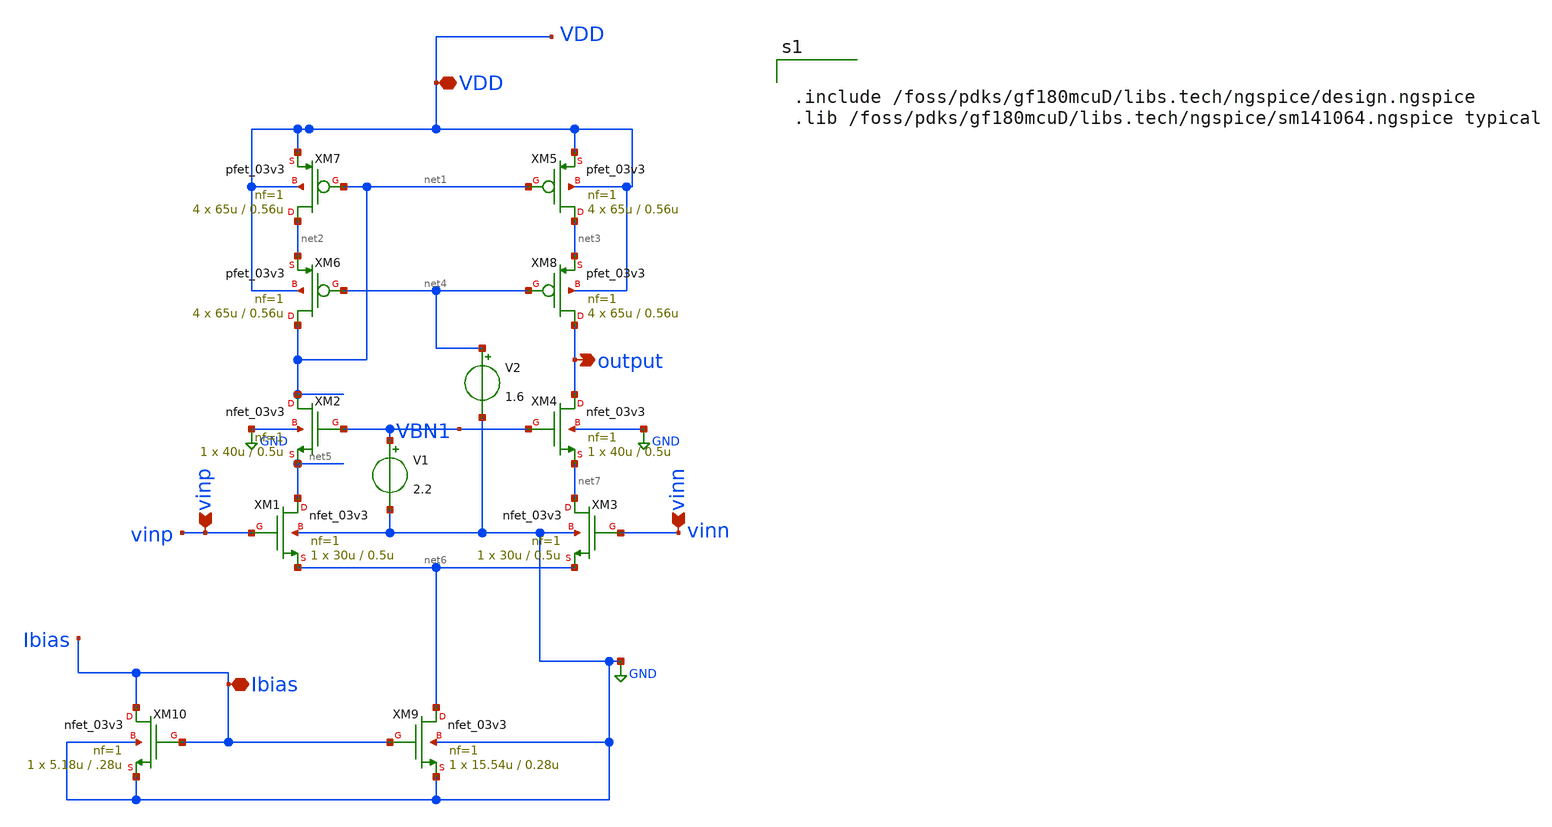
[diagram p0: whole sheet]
** sch_path: designs/libs/core_amps/ota_telescopic/telescopic_cascode.sch
**.subckt telescopic_cascode vinp vinn output Ibias VDD
*.ipin vinp
*.ipin vinn
*.opin output
*.iopin Ibias
*.iopin VDD
XM8 output net4 net3 VDD pfet_03v3 L=0.56u W=65u nf=1 ad='int((nf+1)/2) * W/nf * 0.18u' as='int((nf+2)/2) * W/nf * 0.18u'
+ pd='2*int((nf+1)/2) * (W/nf + 0.18u)' ps='2*int((nf+2)/2) * (W/nf + 0.18u)' nrd='0.18u / W' nrs='0.18u / W'
+ sa=0 sb=0 sd=0 m=4
XM4 output VBN1 net7 GND nfet_03v3 L=0.5u W=40u nf=1 ad='int((nf+1)/2) * W/nf * 0.18u' as='int((nf+2)/2) * W/nf * 0.18u'
+ pd='2*int((nf+1)/2) * (W/nf + 0.18u)' ps='2*int((nf+2)/2) * (W/nf + 0.18u)' nrd='0.18u / W' nrs='0.18u / W'
+ sa=0 sb=0 sd=0 m=1
XM1 net5 vinp net6 GND nfet_03v3 L=0.5u W=30u nf=1 ad='int((nf+1)/2) * W/nf * 0.18u' as='int((nf+2)/2) * W/nf * 0.18u'
+ pd='2*int((nf+1)/2) * (W/nf + 0.18u)' ps='2*int((nf+2)/2) * (W/nf + 0.18u)' nrd='0.18u / W' nrs='0.18u / W'
+ sa=0 sb=0 sd=0 m=1
XM2 net1 VBN1 net5 GND nfet_03v3 L=0.5u W=40u nf=1 ad='int((nf+1)/2) * W/nf * 0.18u' as='int((nf+2)/2) * W/nf * 0.18u'
+ pd='2*int((nf+1)/2) * (W/nf + 0.18u)' ps='2*int((nf+2)/2) * (W/nf + 0.18u)' nrd='0.18u / W' nrs='0.18u / W'
+ sa=0 sb=0 sd=0 m=1
XM3 net7 vinn net6 GND nfet_03v3 L=0.5u W=30u nf=1 ad='int((nf+1)/2) * W/nf * 0.18u' as='int((nf+2)/2) * W/nf * 0.18u'
+ pd='2*int((nf+1)/2) * (W/nf + 0.18u)' ps='2*int((nf+2)/2) * (W/nf + 0.18u)' nrd='0.18u / W' nrs='0.18u / W'
+ sa=0 sb=0 sd=0 m=1
XM5 net3 net1 VDD VDD pfet_03v3 L=0.56u W=65u nf=1 ad='int((nf+1)/2) * W/nf * 0.18u' as='int((nf+2)/2) * W/nf * 0.18u'
+ pd='2*int((nf+1)/2) * (W/nf + 0.18u)' ps='2*int((nf+2)/2) * (W/nf + 0.18u)' nrd='0.18u / W' nrs='0.18u / W'
+ sa=0 sb=0 sd=0 m=4
XM6 net1 net4 net2 VDD pfet_03v3 L=0.56u W=65u nf=1 ad='int((nf+1)/2) * W/nf * 0.18u' as='int((nf+2)/2) * W/nf * 0.18u'
+ pd='2*int((nf+1)/2) * (W/nf + 0.18u)' ps='2*int((nf+2)/2) * (W/nf + 0.18u)' nrd='0.18u / W' nrs='0.18u / W'
+ sa=0 sb=0 sd=0 m=4
XM7 net2 net1 VDD VDD pfet_03v3 L=0.56u W=65u nf=1 ad='int((nf+1)/2) * W/nf * 0.18u' as='int((nf+2)/2) * W/nf * 0.18u'
+ pd='2*int((nf+1)/2) * (W/nf + 0.18u)' ps='2*int((nf+2)/2) * (W/nf + 0.18u)' nrd='0.18u / W' nrs='0.18u / W'
+ sa=0 sb=0 sd=0 m=4
XM9 net6 Ibias GND GND nfet_03v3 L=0.28u W=15.54u nf=1 ad='int((nf+1)/2) * W/nf * 0.18u' as='int((nf+2)/2) * W/nf * 0.18u'
+ pd='2*int((nf+1)/2) * (W/nf + 0.18u)' ps='2*int((nf+2)/2) * (W/nf + 0.18u)' nrd='0.18u / W' nrs='0.18u / W'
+ sa=0 sb=0 sd=0 m=1
XM10 Ibias Ibias GND GND nfet_03v3 L=.28u W=5.18u nf=1 ad='int((nf+1)/2) * W/nf * 0.18u' as='int((nf+2)/2) * W/nf * 0.18u'
+ pd='2*int((nf+1)/2) * (W/nf + 0.18u)' ps='2*int((nf+2)/2) * (W/nf + 0.18u)' nrd='0.18u / W' nrs='0.18u / W'
+ sa=0 sb=0 sd=0 m=1
V1 VBN1 GND 2.2
V2 net4 GND 1.6
**** begin user architecture code


.include /foss/pdks/gf180mcuD/libs.tech/ngspice/design.ngspice
.lib /foss/pdks/gf180mcuD/libs.tech/ngspice/sm141064.ngspice typical

**** end user architecture code
**.ends
.GLOBAL GND
.end
